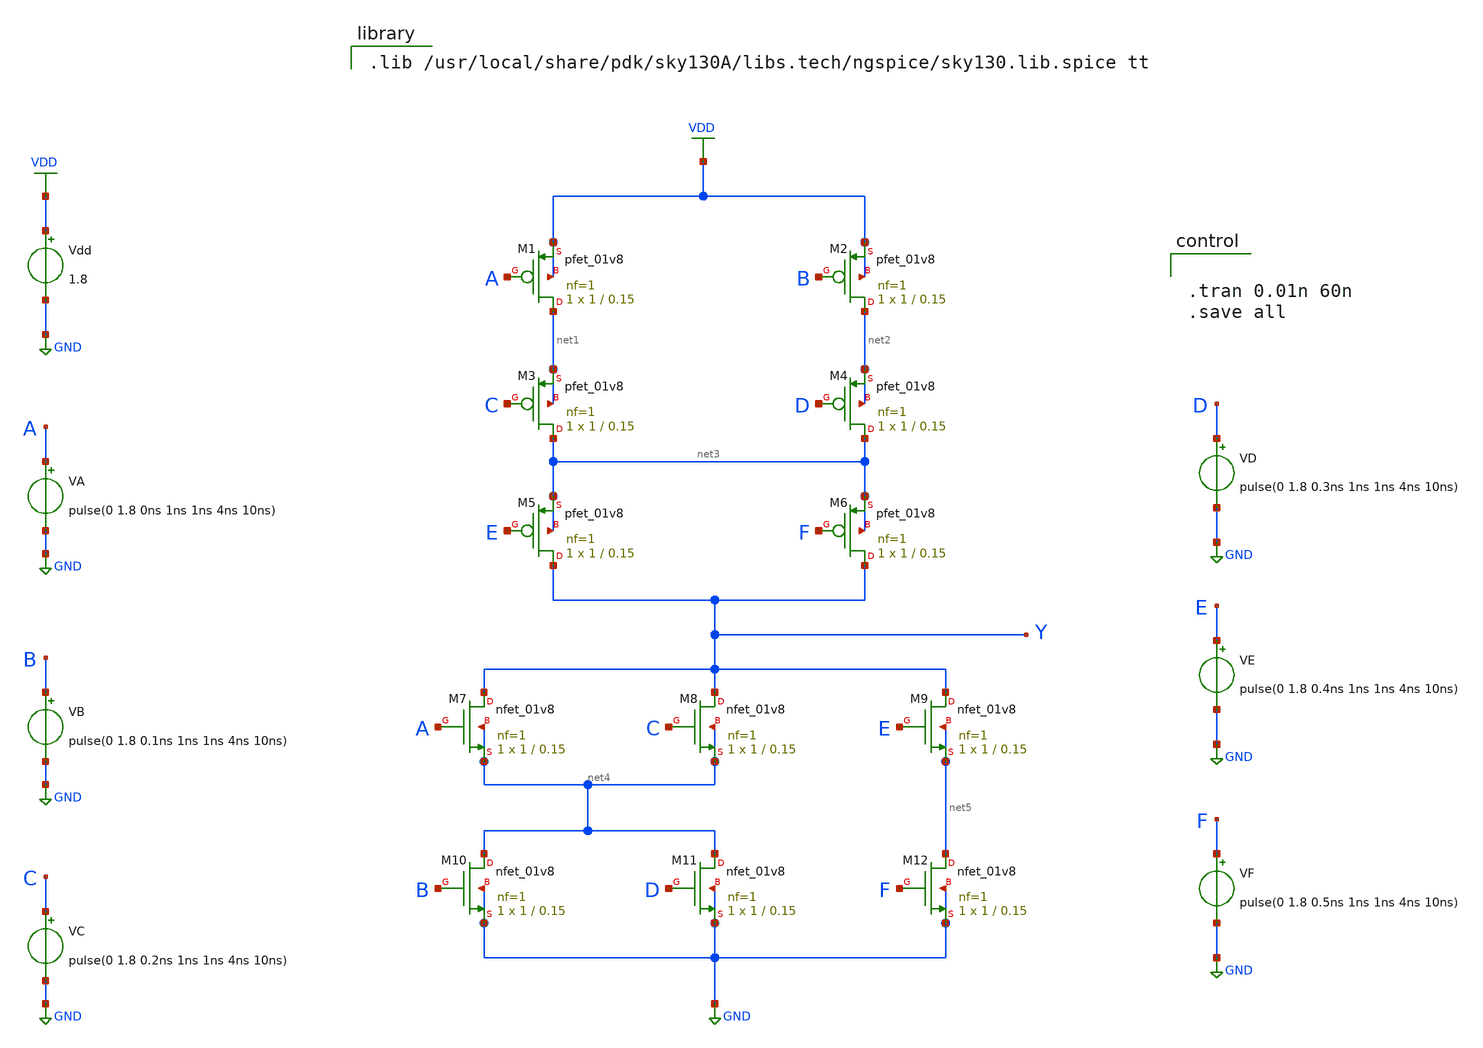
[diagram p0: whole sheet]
** sch_path: Week-2/Function_Pre-Layout/function.sch
**.subckt function
XM1 net1 A VDD VDD sky130_fd_pr__pfet_01v8 L=0.15 W=1 nf=1 ad='int((nf+1)/2) * W/nf * 0.29' as='int((nf+2)/2) * W/nf * 0.29'
+ pd='2*int((nf+1)/2) * (W/nf + 0.29)' ps='2*int((nf+2)/2) * (W/nf + 0.29)' nrd='0.29 / W' nrs='0.29 / W'
+ sa=0 sb=0 sd=0 mult=1 m=1
XM2 net2 B VDD VDD sky130_fd_pr__pfet_01v8 L=0.15 W=1 nf=1 ad='int((nf+1)/2) * W/nf * 0.29' as='int((nf+2)/2) * W/nf * 0.29'
+ pd='2*int((nf+1)/2) * (W/nf + 0.29)' ps='2*int((nf+2)/2) * (W/nf + 0.29)' nrd='0.29 / W' nrs='0.29 / W'
+ sa=0 sb=0 sd=0 mult=1 m=1
XM3 net3 C net1 net1 sky130_fd_pr__pfet_01v8 L=0.15 W=1 nf=1 ad='int((nf+1)/2) * W/nf * 0.29' as='int((nf+2)/2) * W/nf * 0.29'
+ pd='2*int((nf+1)/2) * (W/nf + 0.29)' ps='2*int((nf+2)/2) * (W/nf + 0.29)' nrd='0.29 / W' nrs='0.29 / W'
+ sa=0 sb=0 sd=0 mult=1 m=1
XM4 net3 D net2 net2 sky130_fd_pr__pfet_01v8 L=0.15 W=1 nf=1 ad='int((nf+1)/2) * W/nf * 0.29' as='int((nf+2)/2) * W/nf * 0.29'
+ pd='2*int((nf+1)/2) * (W/nf + 0.29)' ps='2*int((nf+2)/2) * (W/nf + 0.29)' nrd='0.29 / W' nrs='0.29 / W'
+ sa=0 sb=0 sd=0 mult=1 m=1
XM5 Y E net3 net3 sky130_fd_pr__pfet_01v8 L=0.15 W=1 nf=1 ad='int((nf+1)/2) * W/nf * 0.29' as='int((nf+2)/2) * W/nf * 0.29'
+ pd='2*int((nf+1)/2) * (W/nf + 0.29)' ps='2*int((nf+2)/2) * (W/nf + 0.29)' nrd='0.29 / W' nrs='0.29 / W'
+ sa=0 sb=0 sd=0 mult=1 m=1
XM6 Y F net3 net3 sky130_fd_pr__pfet_01v8 L=0.15 W=1 nf=1 ad='int((nf+1)/2) * W/nf * 0.29' as='int((nf+2)/2) * W/nf * 0.29'
+ pd='2*int((nf+1)/2) * (W/nf + 0.29)' ps='2*int((nf+2)/2) * (W/nf + 0.29)' nrd='0.29 / W' nrs='0.29 / W'
+ sa=0 sb=0 sd=0 mult=1 m=1
XM7 Y A net4 net4 sky130_fd_pr__nfet_01v8 L=0.15 W=1 nf=1 ad='int((nf+1)/2) * W/nf * 0.29' as='int((nf+2)/2) * W/nf * 0.29'
+ pd='2*int((nf+1)/2) * (W/nf + 0.29)' ps='2*int((nf+2)/2) * (W/nf + 0.29)' nrd='0.29 / W' nrs='0.29 / W'
+ sa=0 sb=0 sd=0 mult=1 m=1
XM8 Y C net4 net4 sky130_fd_pr__nfet_01v8 L=0.15 W=1 nf=1 ad='int((nf+1)/2) * W/nf * 0.29' as='int((nf+2)/2) * W/nf * 0.29'
+ pd='2*int((nf+1)/2) * (W/nf + 0.29)' ps='2*int((nf+2)/2) * (W/nf + 0.29)' nrd='0.29 / W' nrs='0.29 / W'
+ sa=0 sb=0 sd=0 mult=1 m=1
XM9 Y E net5 net5 sky130_fd_pr__nfet_01v8 L=0.15 W=1 nf=1 ad='int((nf+1)/2) * W/nf * 0.29' as='int((nf+2)/2) * W/nf * 0.29'
+ pd='2*int((nf+1)/2) * (W/nf + 0.29)' ps='2*int((nf+2)/2) * (W/nf + 0.29)' nrd='0.29 / W' nrs='0.29 / W'
+ sa=0 sb=0 sd=0 mult=1 m=1
XM10 net4 B GND GND sky130_fd_pr__nfet_01v8 L=0.15 W=1 nf=1 ad='int((nf+1)/2) * W/nf * 0.29' as='int((nf+2)/2) * W/nf * 0.29'
+ pd='2*int((nf+1)/2) * (W/nf + 0.29)' ps='2*int((nf+2)/2) * (W/nf + 0.29)' nrd='0.29 / W' nrs='0.29 / W'
+ sa=0 sb=0 sd=0 mult=1 m=1
XM11 net4 D GND GND sky130_fd_pr__nfet_01v8 L=0.15 W=1 nf=1 ad='int((nf+1)/2) * W/nf * 0.29' as='int((nf+2)/2) * W/nf * 0.29'
+ pd='2*int((nf+1)/2) * (W/nf + 0.29)' ps='2*int((nf+2)/2) * (W/nf + 0.29)' nrd='0.29 / W' nrs='0.29 / W'
+ sa=0 sb=0 sd=0 mult=1 m=1
XM12 net5 F GND GND sky130_fd_pr__nfet_01v8 L=0.15 W=1 nf=1 ad='int((nf+1)/2) * W/nf * 0.29' as='int((nf+2)/2) * W/nf * 0.29'
+ pd='2*int((nf+1)/2) * (W/nf + 0.29)' ps='2*int((nf+2)/2) * (W/nf + 0.29)' nrd='0.29 / W' nrs='0.29 / W'
+ sa=0 sb=0 sd=0 mult=1 m=1
VA A GND pulse(0 1.8 0ns 1ns 1ns 4ns 10ns)
VB B GND pulse(0 1.8 0.1ns 1ns 1ns 4ns 10ns)
VC C GND pulse(0 1.8 0.2ns 1ns 1ns 4ns 10ns)
VD D GND pulse(0 1.8 0.3ns 1ns 1ns 4ns 10ns)
VE E GND pulse(0 1.8 0.4ns 1ns 1ns 4ns 10ns)
VF F GND pulse(0 1.8 0.5ns 1ns 1ns 4ns 10ns)
Vdd VDD GND 1.8
**** begin user architecture code

.lib /usr/local/share/pdk/sky130A/libs.tech/ngspice/sky130.lib.spice tt



.tran 0.01n 60n
.save all


**** end user architecture code
**.ends
.GLOBAL VDD
.GLOBAL GND
.end
